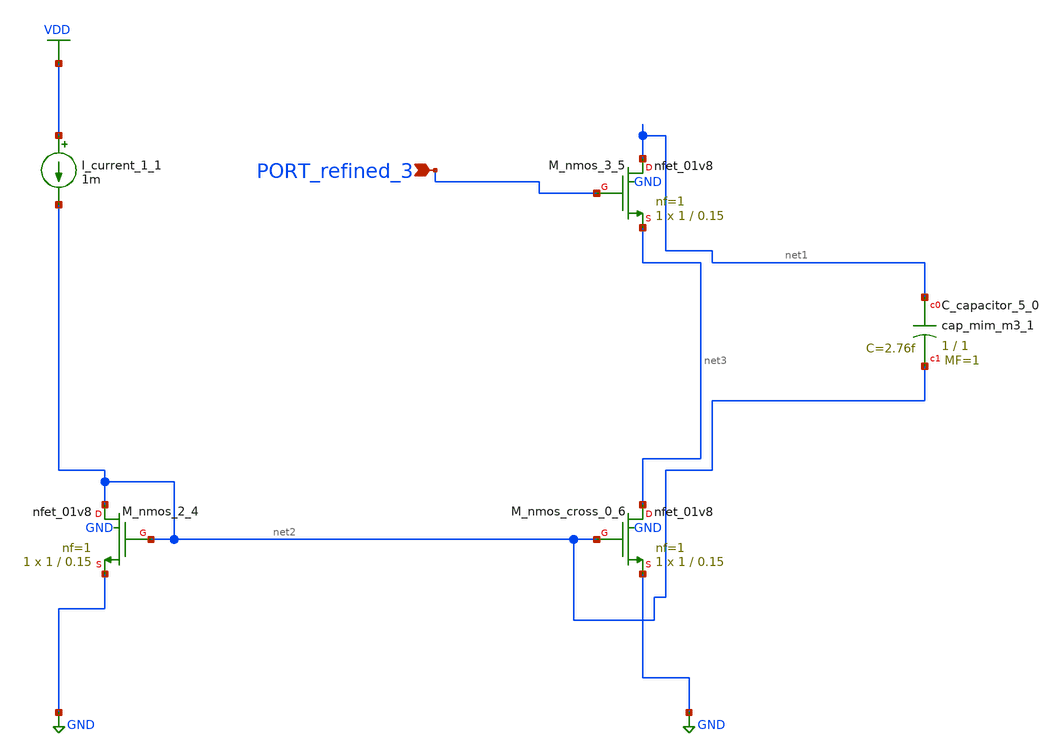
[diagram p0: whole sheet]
** sch_path: schematics/AMSNet/344.sch
**.subckt 344 PORT_refined_3
*.ipin PORT_refined_3
XC_capacitor_5_0 net1 net2 sky130_fd_pr__cap_mim_m3_1 W=1 L=1 MF=1 m=1
I_current_1_1 VDD net2 1m
XM_nmos_2_4 net2 net2 GND GND sky130_fd_pr__nfet_01v8 L=0.15 W=1 nf=1 ad='int((1 + 1)/2) * 1 / 1 * 0.29'
+ as='int((1 + 2)/2) * 1 / 1 * 0.29' pd='2*int((1 + 1)/2) * (1 / 1 + 0.29)' ps='2*int((1 + 2)/2) * (1 / 1 + 0.29)'
+ nrd='0.29 / 1 ' nrs='0.29 / 1 ' sa=0 sb=0 sd=0 mult=1 m=1
XM_nmos_3_5 net1 PORT_refined_3 net3 GND sky130_fd_pr__nfet_01v8 L=0.15 W=1 nf=1 ad='int((1 + 1)/2) * 1 / 1 * 0.29'
+ as='int((1 + 2)/2) * 1 / 1 * 0.29' pd='2*int((1 + 1)/2) * (1 / 1 + 0.29)' ps='2*int((1 + 2)/2) * (1 / 1 + 0.29)'
+ nrd='0.29 / 1 ' nrs='0.29 / 1 ' sa=0 sb=0 sd=0 mult=1 m=1
XM_nmos_cross_0_6 net3 net2 GND GND sky130_fd_pr__nfet_01v8 L=0.15 W=1 nf=1 ad='int((1 + 1)/2) * 1 / 1 * 0.29'
+ as='int((1 + 2)/2) * 1 / 1 * 0.29' pd='2*int((1 + 1)/2) * (1 / 1 + 0.29)' ps='2*int((1 + 2)/2) * (1 / 1 + 0.29)'
+ nrd='0.29 / 1 ' nrs='0.29 / 1 ' sa=0 sb=0 sd=0 mult=1 m=1
**.ends
.GLOBAL GND
.GLOBAL VDD
.end
